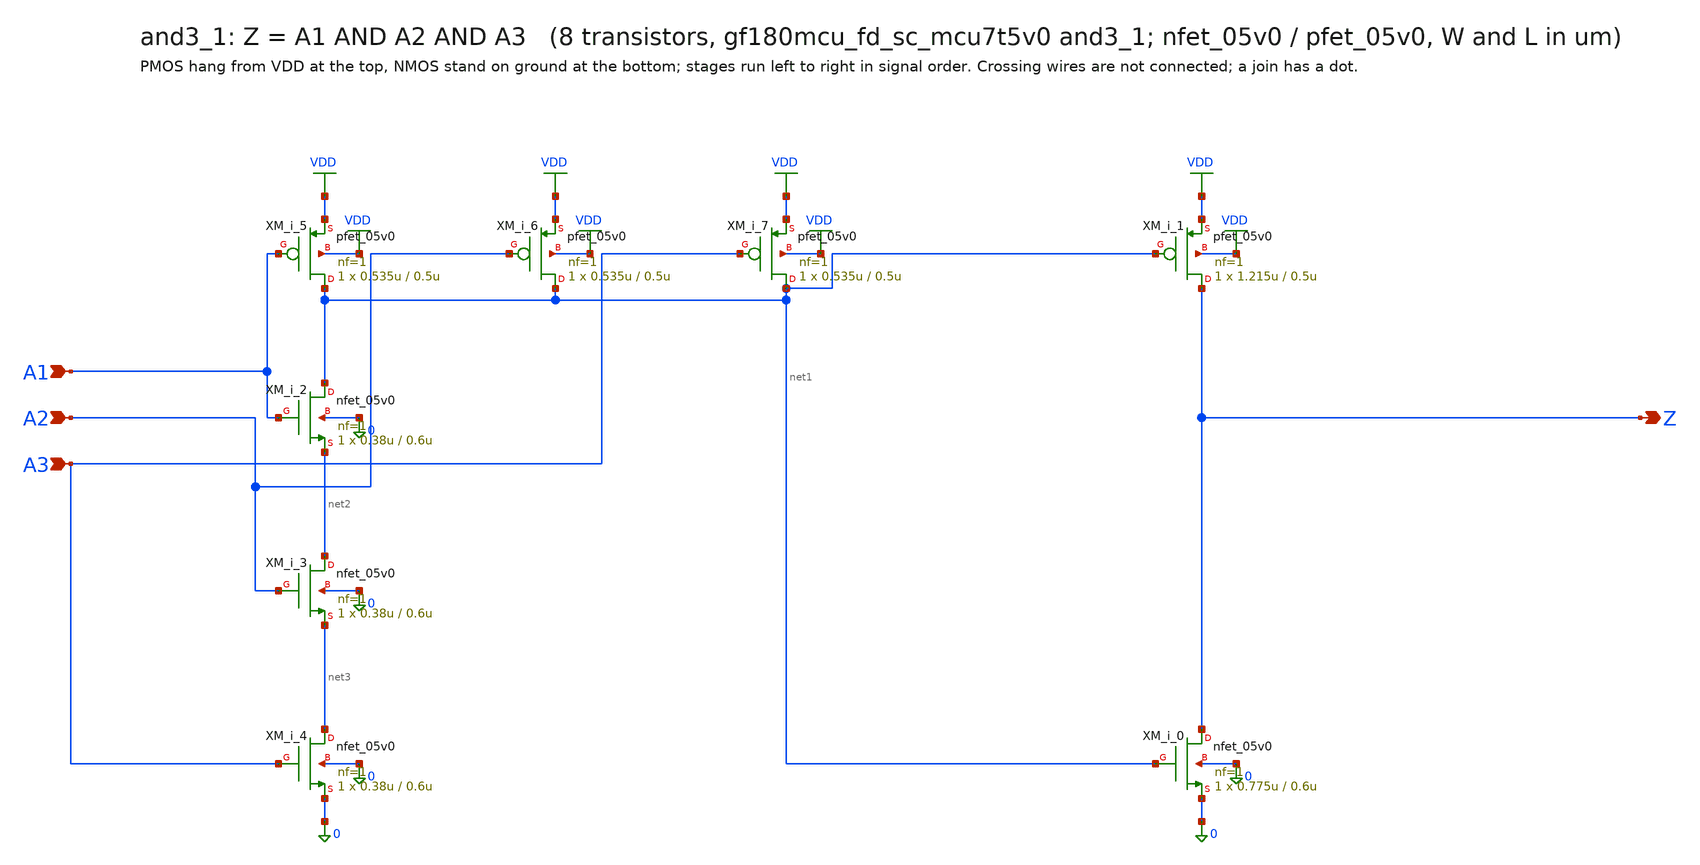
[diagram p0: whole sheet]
** sch_path: xschem/cells_tx/and3_1.sch
**.subckt and3_1 A1 A2 A3 Z
*.ipin A1
*.ipin A2
*.ipin A3
*.opin Z
XM_i_2 net1 A1 net2 0 nfet_05v0 L=0.6u W=0.38u nf=1 ad=1.9e-13 as=1.9e-13 pd=1.76e-06 ps=1.76e-06
+ nrd=0 nrs=0 sa=0 sb=0 sd=0 m=1
XM_i_3 net2 A2 net3 0 nfet_05v0 L=0.6u W=0.38u nf=1 ad=1.9e-13 as=1.9e-13 pd=1.76e-06 ps=1.76e-06
+ nrd=0 nrs=0 sa=0 sb=0 sd=0 m=1
XM_i_4 net3 A3 0 0 nfet_05v0 L=0.6u W=0.38u nf=1 ad=1.9e-13 as=1.9e-13 pd=1.76e-06 ps=1.76e-06 nrd=0
+ nrs=0 sa=0 sb=0 sd=0 m=1
XM_i_0 Z net1 0 0 nfet_05v0 L=0.6u W=0.775u nf=1 ad=3.875e-13 as=3.875e-13 pd=2.55e-06 ps=2.55e-06
+ nrd=0 nrs=0 sa=0 sb=0 sd=0 m=1
XM_i_5 net1 A1 VDD VDD pfet_05v0 L=0.5u W=0.535u nf=1 ad=2.675e-13 as=2.675e-13 pd=2.07e-06
+ ps=2.07e-06 nrd=0 nrs=0 sa=0 sb=0 sd=0 m=1
XM_i_6 net1 A2 VDD VDD pfet_05v0 L=0.5u W=0.535u nf=1 ad=2.675e-13 as=2.675e-13 pd=2.07e-06
+ ps=2.07e-06 nrd=0 nrs=0 sa=0 sb=0 sd=0 m=1
XM_i_7 net1 A3 VDD VDD pfet_05v0 L=0.5u W=0.535u nf=1 ad=2.675e-13 as=2.675e-13 pd=2.07e-06
+ ps=2.07e-06 nrd=0 nrs=0 sa=0 sb=0 sd=0 m=1
XM_i_1 Z net1 VDD VDD pfet_05v0 L=0.5u W=1.215u nf=1 ad=6.075e-13 as=6.075e-13 pd=3.43e-06
+ ps=3.43e-06 nrd=0 nrs=0 sa=0 sb=0 sd=0 m=1
**.ends
.GLOBAL VDD
.end
